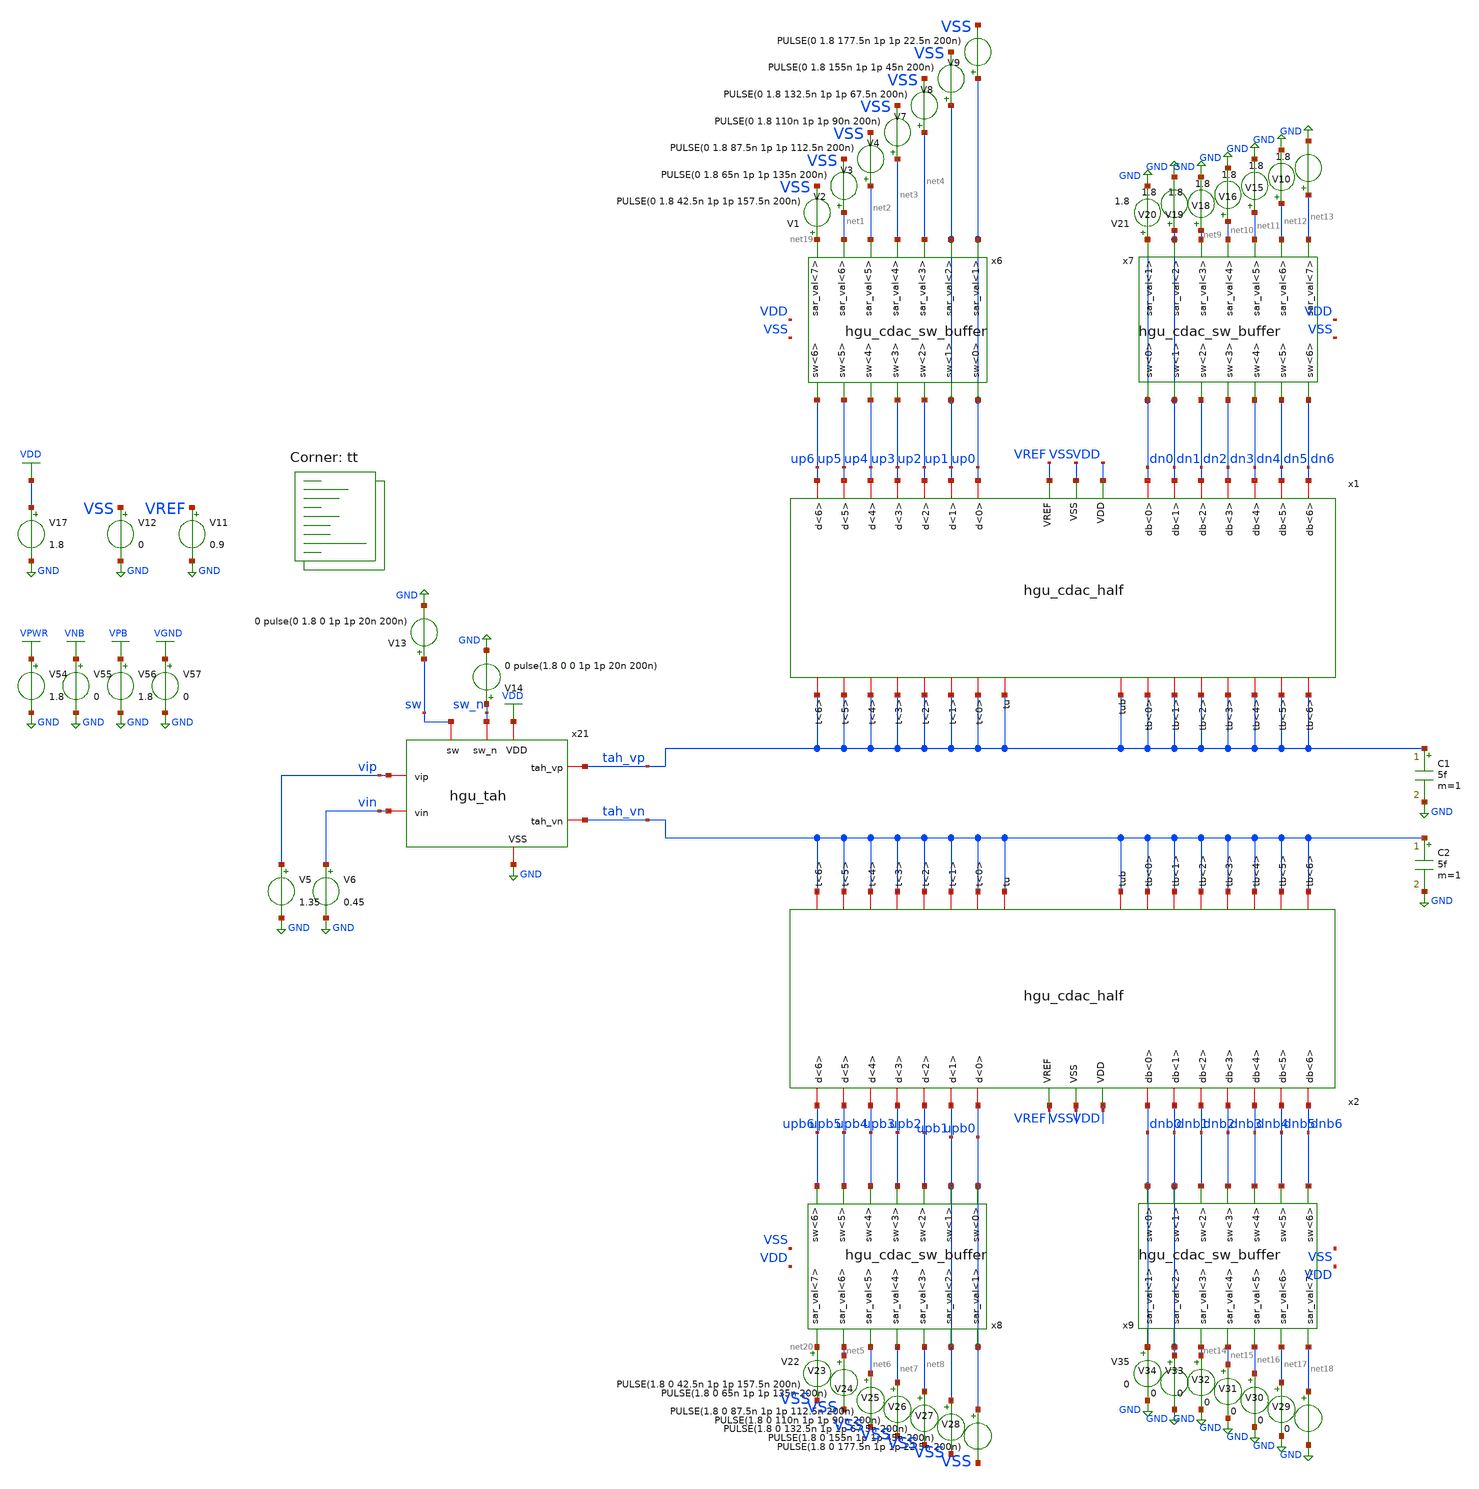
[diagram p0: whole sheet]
** sch_path: hgu/tb/tb_hgu_cdac_8bit.sch
**.subckt tb_hgu_cdac_8bit
x1 up5 dn4 up3 dn1 dn2 up2 dn6 dn5 dn0 up4 up6 up1 up0 dn3 VSS VREF tah_vp tah_vp tah_vp tah_vp
+ tah_vp tah_vp tah_vp tah_vp tah_vp tah_vp tah_vp tah_vp tah_vp tah_vp tah_vp tah_vp VDD hgu_cdac_half
x2 upb5 dnb4 upb3 dnb1 dnb2 upb2 dnb6 dnb5 dnb0 upb4 upb6 upb1 upb0 dnb3 VSS VREF tah_vn tah_vn
+ tah_vn tah_vn tah_vn tah_vn tah_vn tah_vn tah_vn tah_vn tah_vn tah_vn tah_vn tah_vn tah_vn tah_vn VDD
+ hgu_cdac_half
V1 net19 VSS PULSE(0 1.8 42.5n 1p 1p 157.5n 200n)
V2 net1 VSS PULSE(0 1.8 65n 1p 1p 135n 200n)
C1 tah_vp GND 5f m=1
C2 tah_vn GND 5f m=1
V11 VREF GND 0.9
V12 VSS GND 0
x21 sw VDD GND sw_n tah_vp vip vin tah_vn hgu_tah
V13 sw GND 0 pulse(0 1.8 0 1p 1p 20n 200n)
V14 sw_n GND 0 pulse(1.8 0 0 1p 1p 20n 200n)
V17 VDD GND 1.8
V3 net2 VSS PULSE(0 1.8 87.5n 1p 1p 112.5n 200n)
V4 net3 VSS PULSE(0 1.8 110n 1p 1p 90n 200n)
V7 net4 VSS PULSE(0 1.8 132.5n 1p 1p 67.5n 200n)
V8 up1 VSS PULSE(0 1.8 155n 1p 1p 45n 200n)
V9 up0 VSS PULSE(0 1.8 177.5n 1p 1p 22.5n 200n)
V10 net13 GND 1.8
V15 net12 GND 1.8
V16 net11 GND 1.8
V18 net10 GND 1.8
V19 net9 GND 1.8
V20 dn1 GND 1.8
V21 dn0 GND 1.8
V22 net20 VSS PULSE(1.8 0 42.5n 1p 1p 157.5n 200n)
V23 net5 VSS PULSE(1.8 0 65n 1p 1p 135n 200n)
V24 net6 VSS PULSE(1.8 0 87.5n 1p 1p 112.5n 200n)
V25 net7 VSS PULSE(1.8 0 110n 1p 1p 90n 200n)
V26 net8 VSS PULSE(1.8 0 132.5n 1p 1p 67.5n 200n)
V27 upb1 VSS PULSE(1.8 0 155n 1p 1p 45n 200n)
V28 upb0 VSS PULSE(1.8 0 177.5n 1p 1p 22.5n 200n)
V29 net18 GND 0
V30 net17 GND 0
V31 net16 GND 0
V32 net15 GND 0
V33 net14 GND 0
V34 dnb1 GND 0
V35 dnb0 GND 0
V5 vip GND 1.35
V6 vin GND 0.45
x6 net4 net1 up0 up1 net3 net2 net19 up1 up2 up5 up3 up0 up4 up6 hgu_cdac_sw_buffer
x7 net9 net12 dn0 dn1 net10 net11 net13 dn1 dn2 dn5 dn3 dn0 dn4 dn6 hgu_cdac_sw_buffer
x8 net8 net5 upb0 upb1 net7 net6 net20 upb1 upb2 upb5 upb3 upb0 upb4 upb6 hgu_cdac_sw_buffer
x9 net14 net17 dnb0 dnb1 net15 net16 net18 dnb1 dnb2 dnb5 dnb3 dnb0 dnb4 dnb6 hgu_cdac_sw_buffer
V54 VPWR GND 1.8
V55 VNB GND 0
V56 VPB GND 1.8
V57 VGND GND 0
**** begin user architecture code


.save all
.temp = 25
.tran 100p 200n
.OPTIONS savecurrents

.include /foss/pdks/sky130A/libs.ref/sky130_fd_sc_hd/spice/sky130_fd_sc_hd.spice
.include /foss/designs/hgu_goss/hgu/mag/hgu_cdac_unit.spice
.include /foss/designs/hgu_goss/hgu/spice/hgu_cdac_half_flat.mag.spice


.control
	run
        plot v(up6)+56 v(up5)+54 v(up4)+52 v(up3)+50 v(up2)+48 v(up1)+46 v(up0)+44 v(dn6)+42
+ v(dn5)+40 v(dn4)+38 v(dn3)+36 v(dn2)+34 v(dn1)+32 v(dn0)+30 v(upb6)+28 v(upb5)+26 v(upb4)+24 v(upb3)+22
+ v(upb2)+20 v(upb1)+18 v(upb0)+16 v(dnb6)+14 v(dnb5)+12 v(dnb4)+10 v(dnb3)+8 v(dnb2)+6 v(dnb1)+4 v(dnb0)+2
	plot v(sw) v(tah_vp)-v(tah_vn) vip vin

.endc


.lib $::SKYWATER_MODELS/sky130.lib.spice tt
**** end user architecture code
**.ends
.GLOBAL GND
.GLOBAL VDD
.GLOBAL VGND
.GLOBAL VNB
.GLOBAL VPB
.GLOBAL VPWR
.end
